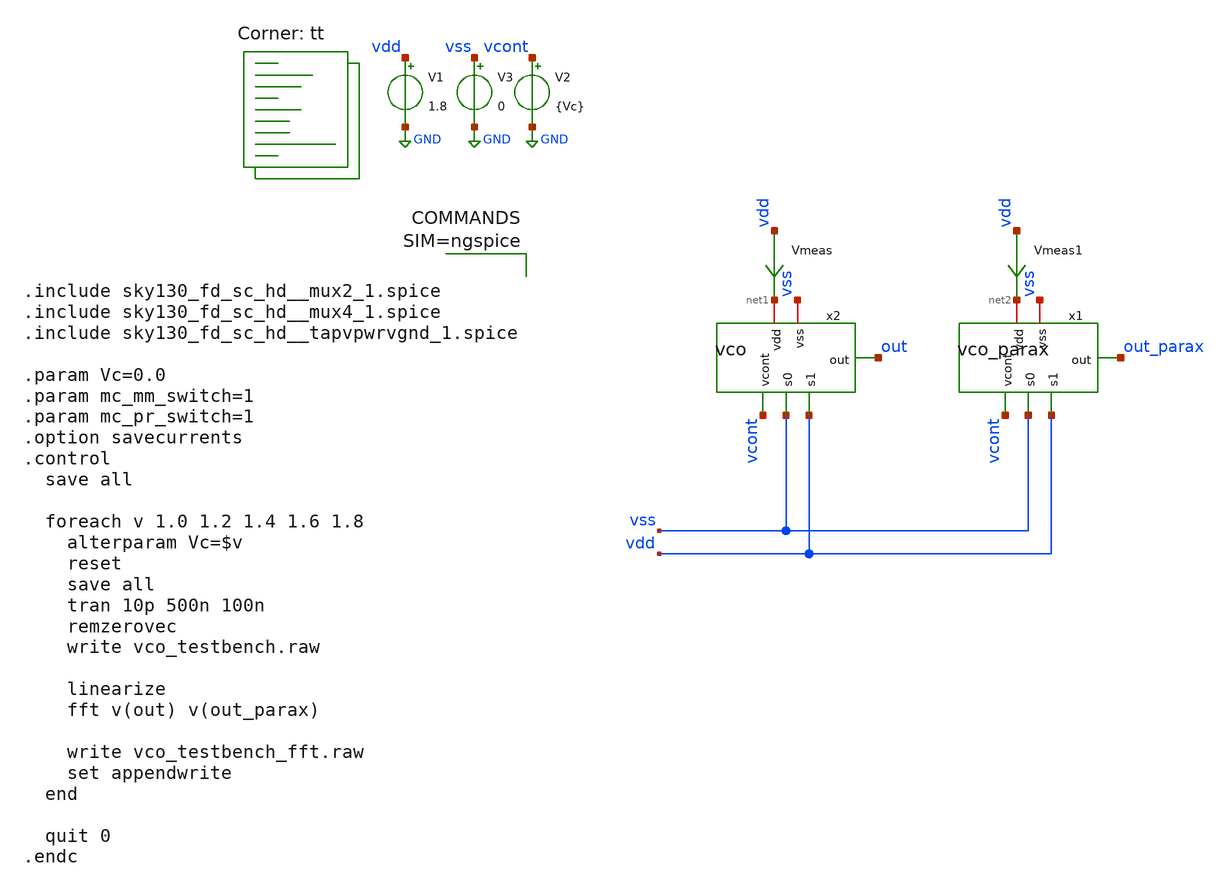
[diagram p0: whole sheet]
** sch_path: xschem/vco_testbench.sch
**.subckt vco_testbench
V1 vdd GND 1.8
V2 vcont GND {Vc}
x2 net1 vcont vss vdd out vss vco
V3 vss GND 0
Vmeas vdd net1 0
.save i(vmeas)
x1 net2 vcont vss vdd out_parax vss vco_parax
Vmeas1 vdd net2 0
.save i(vmeas1)
**** begin user architecture code
.lib $::SKYWATER_MODELS/sky130.lib.spice tt



.include sky130_fd_sc_hd__mux2_1.spice
.include sky130_fd_sc_hd__mux4_1.spice
.include sky130_fd_sc_hd__tapvpwrvgnd_1.spice

.param Vc=0.0
.param mc_mm_switch=1
.param mc_pr_switch=1
.option savecurrents
.control
  save all

  foreach v 1.0 1.2 1.4 1.6 1.8
    alterparam Vc=$v
    reset
    save all
    tran 10p 500n 100n
    remzerovec
    write vco_testbench.raw

    linearize
    fft v(out) v(out_parax)

    write vco_testbench_fft.raw
    set appendwrite
  end

  quit 0
.endc



**** end user architecture code
**.ends

* expanding   symbol:  vco.sym # of pins=6
** sym_path: xschem/vco.sym
** sch_path: xschem/vco.sch
.subckt vco vdd vcont s0 s1 out vss
*.iopin vdd
*.ipin s0
*.ipin s1
*.ipin vcont
*.iopin vss
*.opin out
x1 vdd vcont_b net5 out vcont vss delay_stage
x2 vdd vcont_b net6 net5 vcont vss delay_stage
x3 vdd vcont_b net4 net6 vcont vss delay_stage
x4 vdd vcont_b net7 net4 vcont vss delay_stage
x5 vdd vcont_b net3 net7 vcont vss delay_stage
x6 vdd vcont_b net8 net3 vcont vss delay_stage
x7 vdd vcont_b net2 net8 vcont vss delay_stage
x9 vdd vcont_b net9 net2 vcont vss delay_stage
x10 vdd vcont_b net1 net9 vcont vss delay_stage
x11 net1 net2 net3 net4 s0 s1 vss vss vdd vdd out sky130_fd_sc_hd__mux4_1
XM5 vcont_b vcont_b vdd vdd sky130_fd_pr__pfet_01v8 L=0.3 W=2 nf=1 ad='int((nf+1)/2) * W/nf * 0.29' as='int((nf+2)/2) * W/nf * 0.29'
+ pd='2*int((nf+1)/2) * (W/nf + 0.29)' ps='2*int((nf+2)/2) * (W/nf + 0.29)' nrd='0.29 / W' nrs='0.29 / W'
+ sa=0 sb=0 sd=0 mult=1 m=1
XM1 vcont_b vcont vss vss sky130_fd_pr__nfet_01v8_lvt L=0.3 W=2 nf=1 ad='int((nf+1)/2) * W/nf * 0.29'
+ as='int((nf+2)/2) * W/nf * 0.29' pd='2*int((nf+1)/2) * (W/nf + 0.29)' ps='2*int((nf+2)/2) * (W/nf + 0.29)'
+ nrd='0.29 / W' nrs='0.29 / W' sa=0 sb=0 sd=0 mult=1 m=1
x8 vss vdd sky130_fd_sc_hd__tapvpwrvgnd_1
.ends


* expanding   symbol:  vco_parax.sym # of pins=6
** sym_path: xschem/vco.sym
.include [file normalize ../mag/vco.sim.spice]

* expanding   symbol:  delay_stage.sym # of pins=6
** sym_path: xschem/delay_stage.sym
** sch_path: xschem/delay_stage.sch
.subckt delay_stage vdd vcont_p out in vcont_n vss
*.ipin in
*.opin out
*.iopin vdd
*.ipin vcont_n
*.ipin vcont_p
*.iopin vss
XM3 out in net2 vss sky130_fd_pr__nfet_01v8 L=0.45 W=1 nf=1 ad='int((nf+1)/2) * W/nf * 0.29' as='int((nf+2)/2) * W/nf * 0.29'
+ pd='2*int((nf+1)/2) * (W/nf + 0.29)' ps='2*int((nf+2)/2) * (W/nf + 0.29)' nrd='0.29 / W' nrs='0.29 / W'
+ sa=0 sb=0 sd=0 mult=1 m=1
XM2 out in net1 vdd sky130_fd_pr__pfet_01v8 L=0.45 W=2 nf=1 ad='int((nf+1)/2) * W/nf * 0.29' as='int((nf+2)/2) * W/nf * 0.29'
+ pd='2*int((nf+1)/2) * (W/nf + 0.29)' ps='2*int((nf+2)/2) * (W/nf + 0.29)' nrd='0.29 / W' nrs='0.29 / W'
+ sa=0 sb=0 sd=0 mult=1 m=1
XM1 net1 vcont_p vdd vdd sky130_fd_pr__pfet_01v8 L=0.45 W=2 nf=1 ad='int((nf+1)/2) * W/nf * 0.29' as='int((nf+2)/2) * W/nf * 0.29'
+ pd='2*int((nf+1)/2) * (W/nf + 0.29)' ps='2*int((nf+2)/2) * (W/nf + 0.29)' nrd='0.29 / W' nrs='0.29 / W'
+ sa=0 sb=0 sd=0 mult=1 m=1
XM4 net2 vcont_n vss vss sky130_fd_pr__nfet_01v8 L=0.45 W=1 nf=1 ad='int((nf+1)/2) * W/nf * 0.29' as='int((nf+2)/2) * W/nf * 0.29'
+ pd='2*int((nf+1)/2) * (W/nf + 0.29)' ps='2*int((nf+2)/2) * (W/nf + 0.29)' nrd='0.29 / W' nrs='0.29 / W'
+ sa=0 sb=0 sd=0 mult=1 m=1
.ends

.GLOBAL GND
.end
